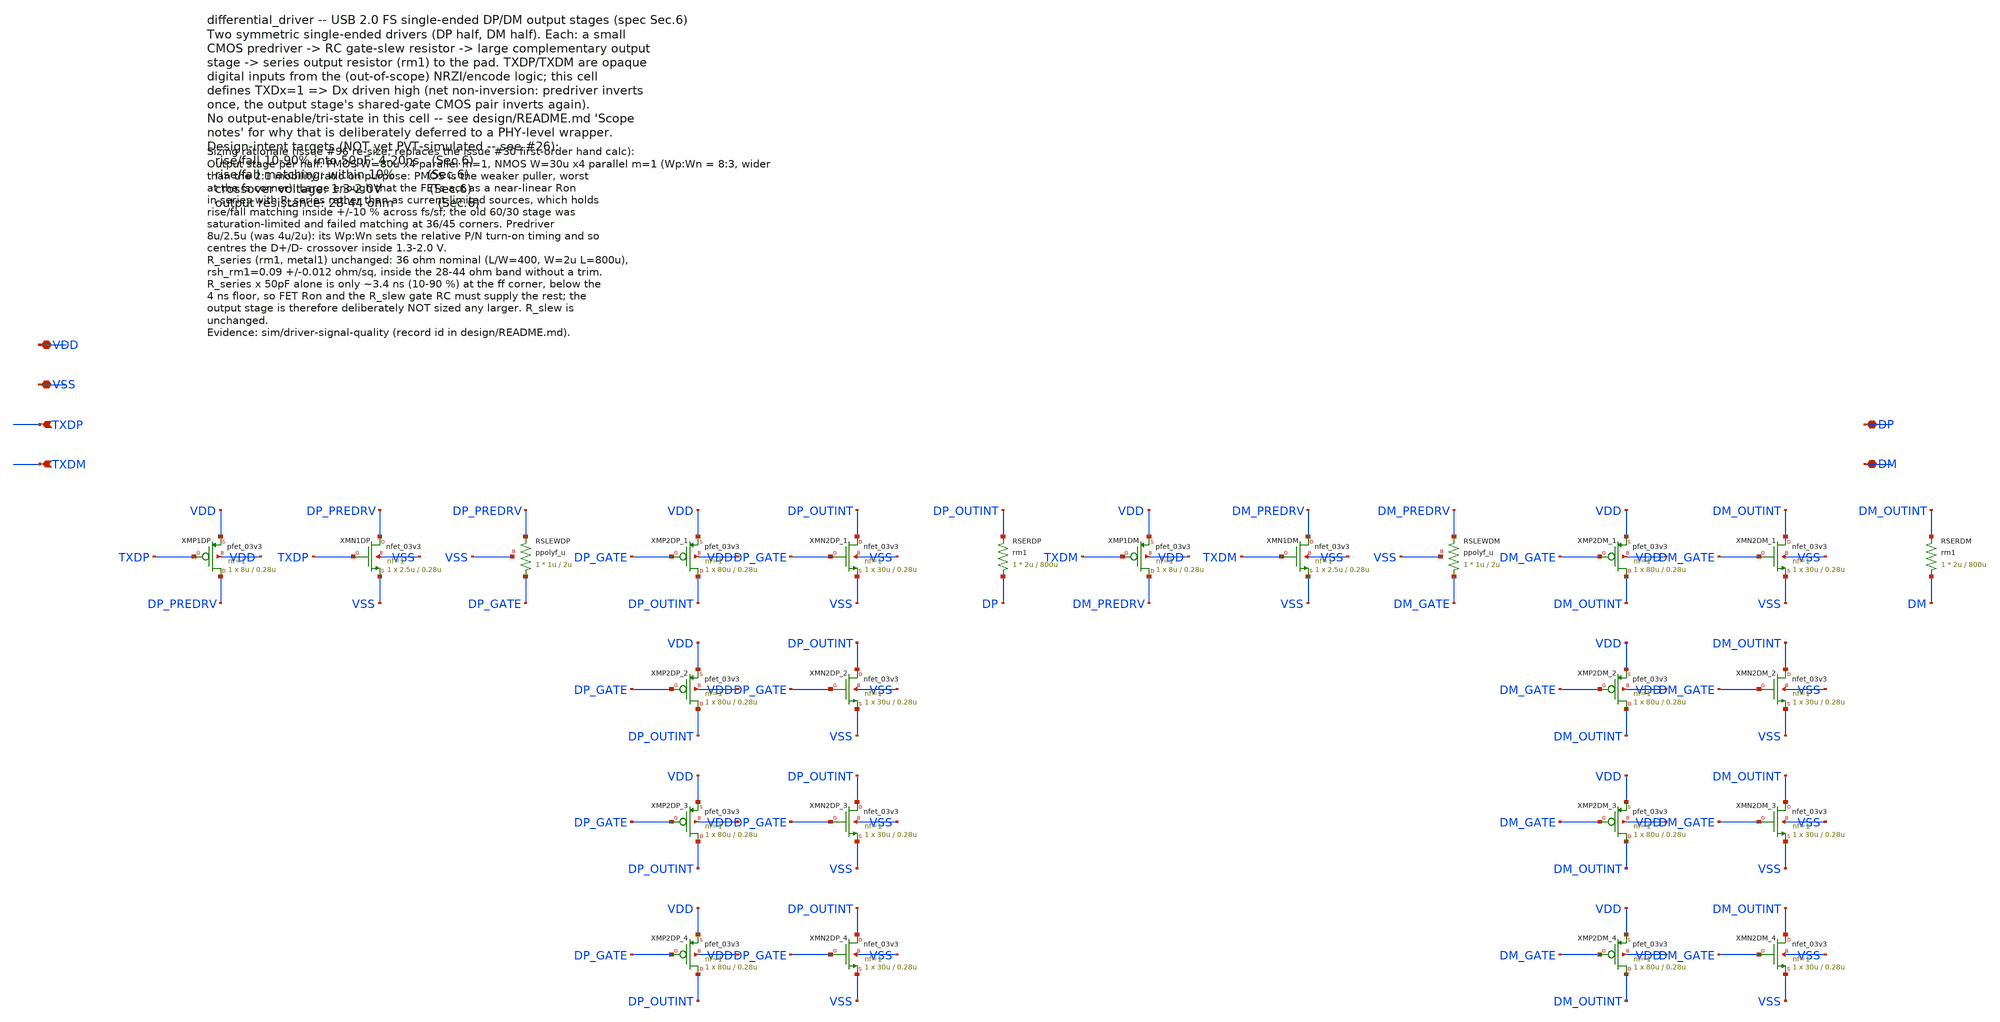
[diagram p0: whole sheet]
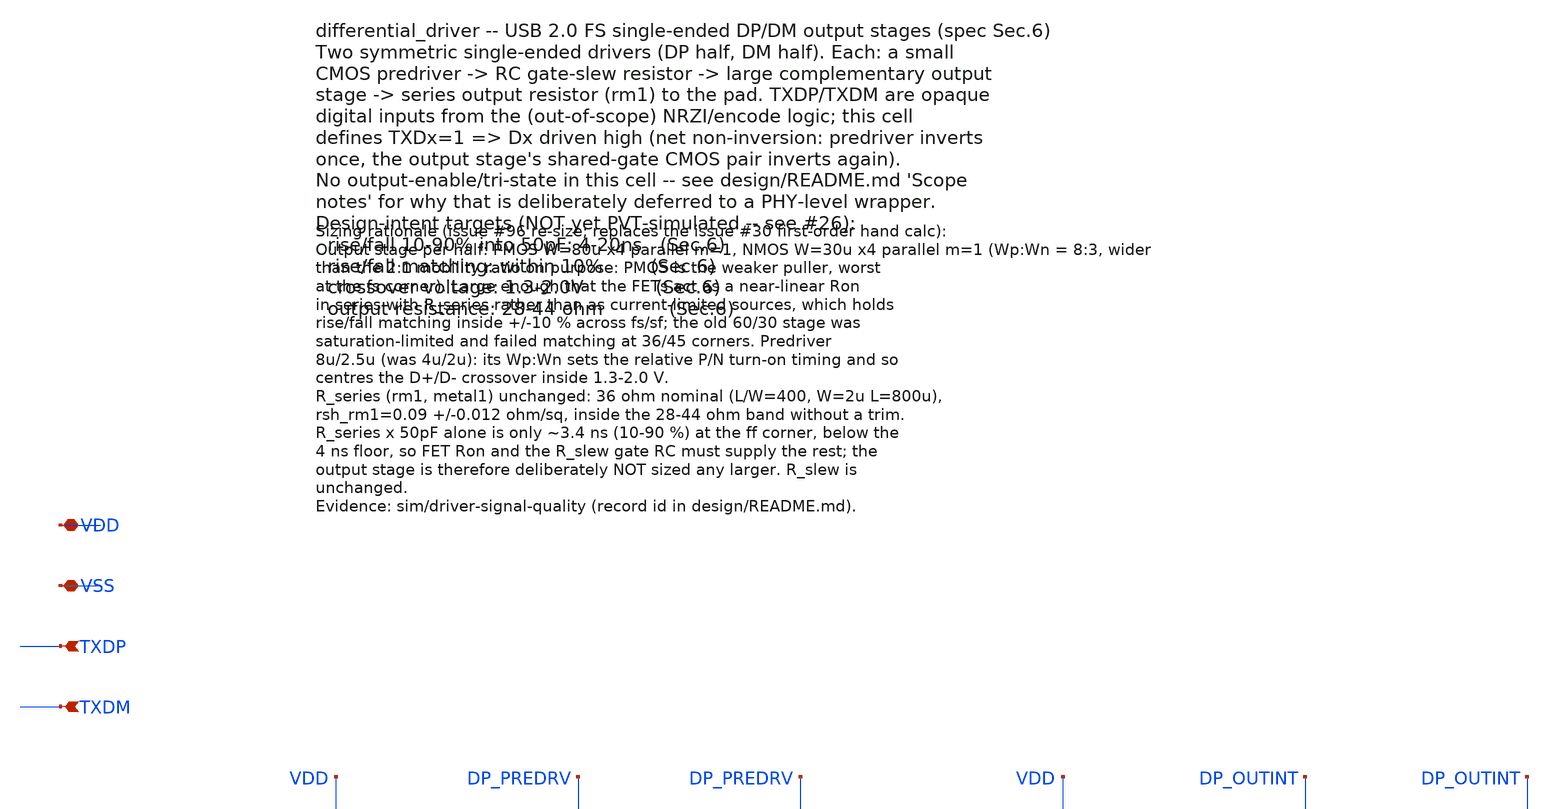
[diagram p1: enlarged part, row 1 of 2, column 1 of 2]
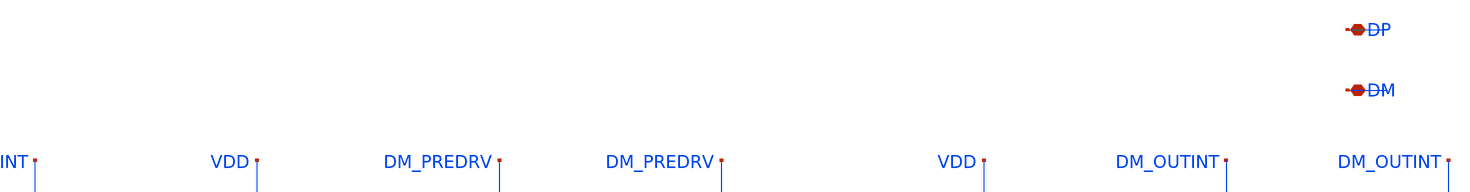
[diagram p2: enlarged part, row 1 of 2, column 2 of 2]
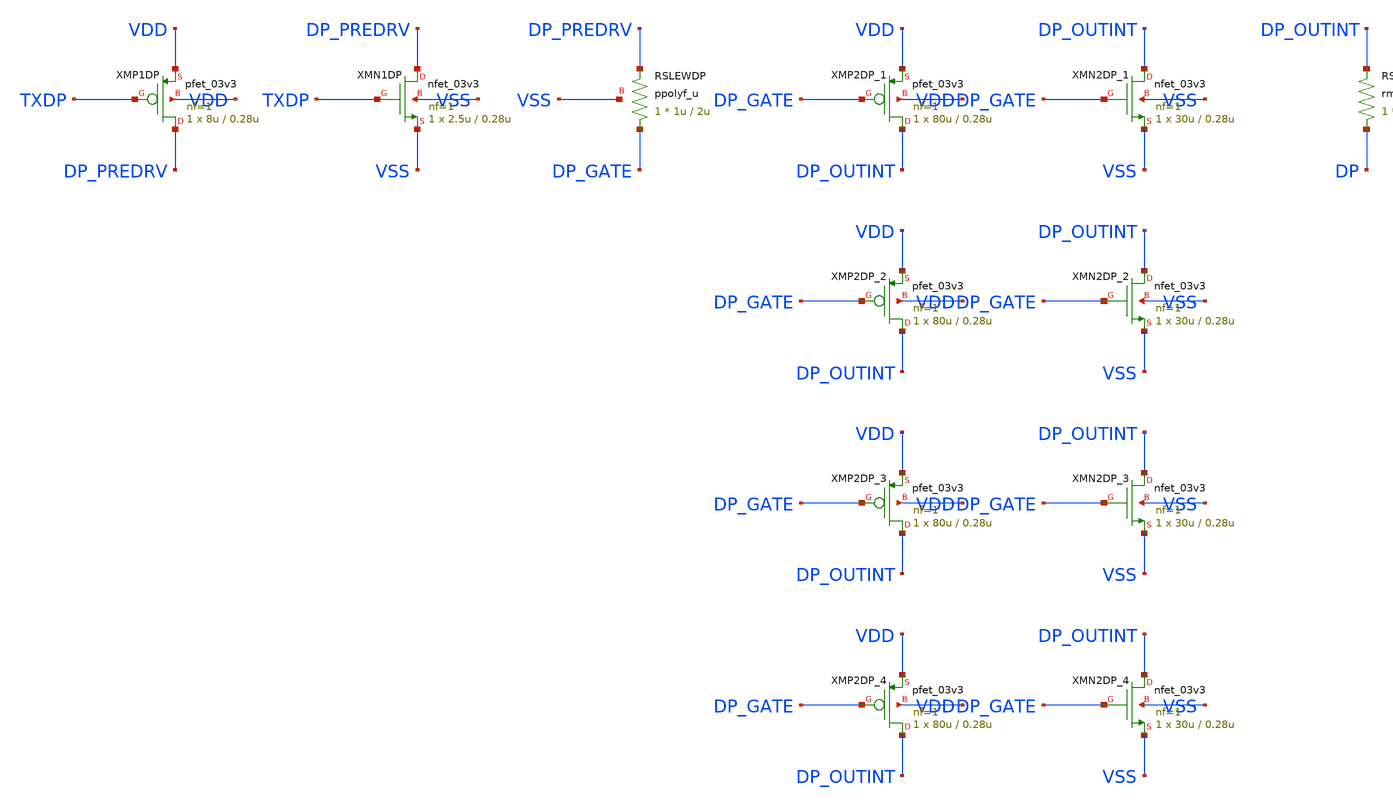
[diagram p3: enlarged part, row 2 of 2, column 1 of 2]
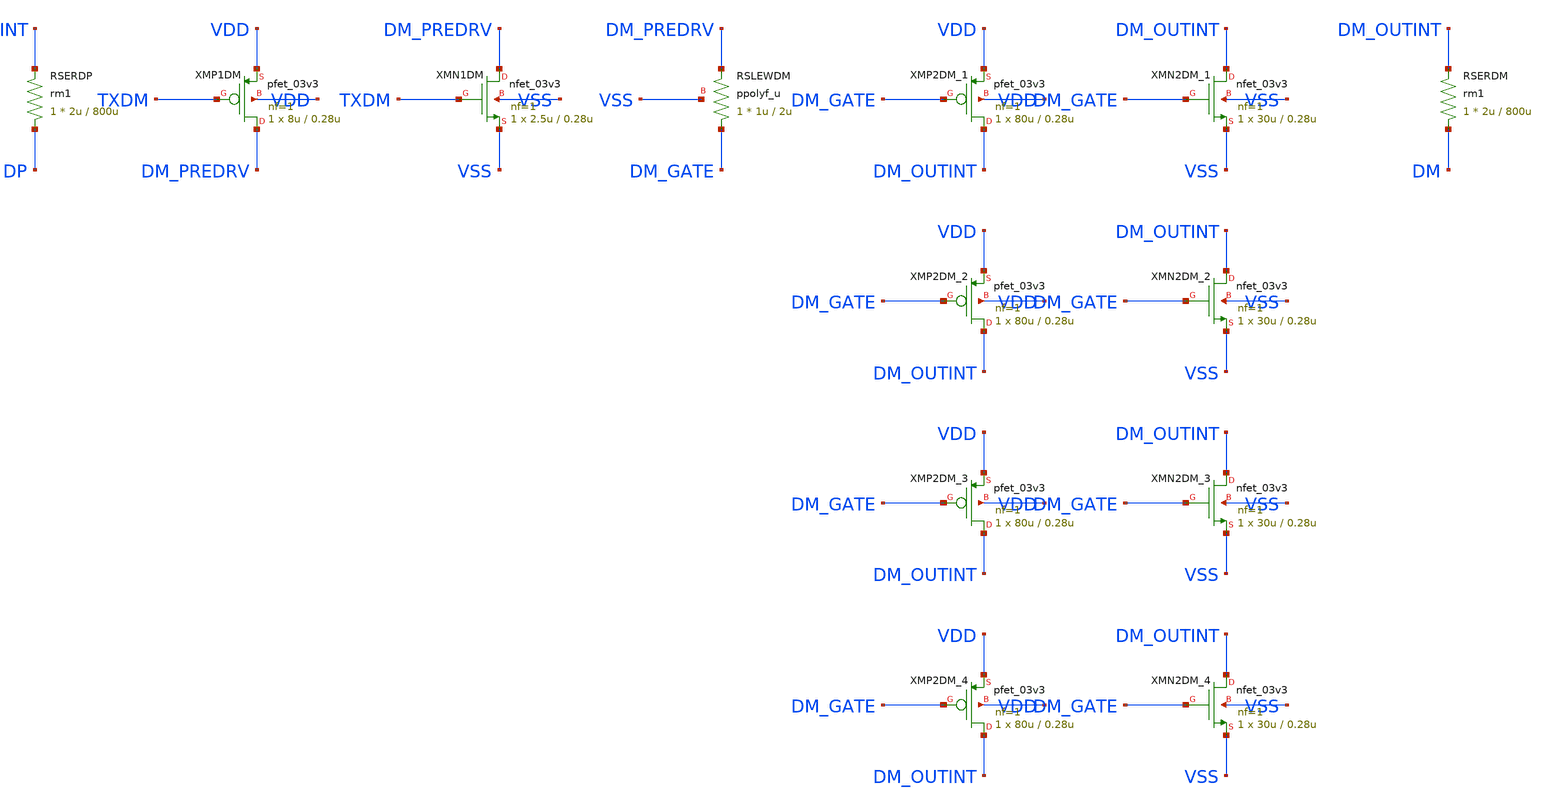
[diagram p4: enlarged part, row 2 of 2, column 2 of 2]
** sch_path: design/differential_driver.sch
**.subckt differential_driver VDD VSS TXDP TXDM DP DM
*.iopin VDD
*.iopin VSS
*.ipin TXDP
*.ipin TXDM
*.iopin DP
*.iopin DM
XMP1DP DP_PREDRV TXDP VDD VDD pfet_03v3 L=0.28u W=8u nf=1 ad='int((nf+1)/2) * W/nf * 0.18u' as='int((nf+2)/2) * W/nf * 0.18u'
+ pd='2*int((nf+1)/2) * (W/nf + 0.18u)' ps='2*int((nf+2)/2) * (W/nf + 0.18u)' nrd='0.18u / W' nrs='0.18u / W'
+ sa=0 sb=0 sd=0 m=1
XMN1DP DP_PREDRV TXDP VSS VSS nfet_03v3 L=0.28u W=2.5u nf=1 ad='int((nf+1)/2) * W/nf * 0.18u' as='int((nf+2)/2) * W/nf * 0.18u'
+ pd='2*int((nf+1)/2) * (W/nf + 0.18u)' ps='2*int((nf+2)/2) * (W/nf + 0.18u)' nrd='0.18u / W' nrs='0.18u / W'
+ sa=0 sb=0 sd=0 m=1
XRSLEWDP DP_GATE DP_PREDRV VSS ppolyf_u r_width=1u r_length=2u m=1
XMP2DP_1 DP_OUTINT DP_GATE VDD VDD pfet_03v3 L=0.28u W=80u nf=1 ad='int((nf+1)/2) * W/nf * 0.18u' as='int((nf+2)/2) * W/nf * 0.18u'
+ pd='2*int((nf+1)/2) * (W/nf + 0.18u)' ps='2*int((nf+2)/2) * (W/nf + 0.18u)' nrd='0.18u / W' nrs='0.18u / W'
+ sa=0 sb=0 sd=0 m=1
XMP2DP_2 DP_OUTINT DP_GATE VDD VDD pfet_03v3 L=0.28u W=80u nf=1 ad='int((nf+1)/2) * W/nf * 0.18u' as='int((nf+2)/2) * W/nf * 0.18u'
+ pd='2*int((nf+1)/2) * (W/nf + 0.18u)' ps='2*int((nf+2)/2) * (W/nf + 0.18u)' nrd='0.18u / W' nrs='0.18u / W'
+ sa=0 sb=0 sd=0 m=1
XMP2DP_3 DP_OUTINT DP_GATE VDD VDD pfet_03v3 L=0.28u W=80u nf=1 ad='int((nf+1)/2) * W/nf * 0.18u' as='int((nf+2)/2) * W/nf * 0.18u'
+ pd='2*int((nf+1)/2) * (W/nf + 0.18u)' ps='2*int((nf+2)/2) * (W/nf + 0.18u)' nrd='0.18u / W' nrs='0.18u / W'
+ sa=0 sb=0 sd=0 m=1
XMP2DP_4 DP_OUTINT DP_GATE VDD VDD pfet_03v3 L=0.28u W=80u nf=1 ad='int((nf+1)/2) * W/nf * 0.18u' as='int((nf+2)/2) * W/nf * 0.18u'
+ pd='2*int((nf+1)/2) * (W/nf + 0.18u)' ps='2*int((nf+2)/2) * (W/nf + 0.18u)' nrd='0.18u / W' nrs='0.18u / W'
+ sa=0 sb=0 sd=0 m=1
XMN2DP_1 DP_OUTINT DP_GATE VSS VSS nfet_03v3 L=0.28u W=30u nf=1 ad='int((nf+1)/2) * W/nf * 0.18u' as='int((nf+2)/2) * W/nf * 0.18u'
+ pd='2*int((nf+1)/2) * (W/nf + 0.18u)' ps='2*int((nf+2)/2) * (W/nf + 0.18u)' nrd='0.18u / W' nrs='0.18u / W'
+ sa=0 sb=0 sd=0 m=1
XMN2DP_2 DP_OUTINT DP_GATE VSS VSS nfet_03v3 L=0.28u W=30u nf=1 ad='int((nf+1)/2) * W/nf * 0.18u' as='int((nf+2)/2) * W/nf * 0.18u'
+ pd='2*int((nf+1)/2) * (W/nf + 0.18u)' ps='2*int((nf+2)/2) * (W/nf + 0.18u)' nrd='0.18u / W' nrs='0.18u / W'
+ sa=0 sb=0 sd=0 m=1
XMN2DP_3 DP_OUTINT DP_GATE VSS VSS nfet_03v3 L=0.28u W=30u nf=1 ad='int((nf+1)/2) * W/nf * 0.18u' as='int((nf+2)/2) * W/nf * 0.18u'
+ pd='2*int((nf+1)/2) * (W/nf + 0.18u)' ps='2*int((nf+2)/2) * (W/nf + 0.18u)' nrd='0.18u / W' nrs='0.18u / W'
+ sa=0 sb=0 sd=0 m=1
XMN2DP_4 DP_OUTINT DP_GATE VSS VSS nfet_03v3 L=0.28u W=30u nf=1 ad='int((nf+1)/2) * W/nf * 0.18u' as='int((nf+2)/2) * W/nf * 0.18u'
+ pd='2*int((nf+1)/2) * (W/nf + 0.18u)' ps='2*int((nf+2)/2) * (W/nf + 0.18u)' nrd='0.18u / W' nrs='0.18u / W'
+ sa=0 sb=0 sd=0 m=1
XRSERDP DP DP_OUTINT rm1 r_width=2u r_length=800u m=1
XMP1DM DM_PREDRV TXDM VDD VDD pfet_03v3 L=0.28u W=8u nf=1 ad='int((nf+1)/2) * W/nf * 0.18u' as='int((nf+2)/2) * W/nf * 0.18u'
+ pd='2*int((nf+1)/2) * (W/nf + 0.18u)' ps='2*int((nf+2)/2) * (W/nf + 0.18u)' nrd='0.18u / W' nrs='0.18u / W'
+ sa=0 sb=0 sd=0 m=1
XMN1DM DM_PREDRV TXDM VSS VSS nfet_03v3 L=0.28u W=2.5u nf=1 ad='int((nf+1)/2) * W/nf * 0.18u' as='int((nf+2)/2) * W/nf * 0.18u'
+ pd='2*int((nf+1)/2) * (W/nf + 0.18u)' ps='2*int((nf+2)/2) * (W/nf + 0.18u)' nrd='0.18u / W' nrs='0.18u / W'
+ sa=0 sb=0 sd=0 m=1
XRSLEWDM DM_GATE DM_PREDRV VSS ppolyf_u r_width=1u r_length=2u m=1
XMP2DM_1 DM_OUTINT DM_GATE VDD VDD pfet_03v3 L=0.28u W=80u nf=1 ad='int((nf+1)/2) * W/nf * 0.18u' as='int((nf+2)/2) * W/nf * 0.18u'
+ pd='2*int((nf+1)/2) * (W/nf + 0.18u)' ps='2*int((nf+2)/2) * (W/nf + 0.18u)' nrd='0.18u / W' nrs='0.18u / W'
+ sa=0 sb=0 sd=0 m=1
XMP2DM_2 DM_OUTINT DM_GATE VDD VDD pfet_03v3 L=0.28u W=80u nf=1 ad='int((nf+1)/2) * W/nf * 0.18u' as='int((nf+2)/2) * W/nf * 0.18u'
+ pd='2*int((nf+1)/2) * (W/nf + 0.18u)' ps='2*int((nf+2)/2) * (W/nf + 0.18u)' nrd='0.18u / W' nrs='0.18u / W'
+ sa=0 sb=0 sd=0 m=1
XMP2DM_3 DM_OUTINT DM_GATE VDD VDD pfet_03v3 L=0.28u W=80u nf=1 ad='int((nf+1)/2) * W/nf * 0.18u' as='int((nf+2)/2) * W/nf * 0.18u'
+ pd='2*int((nf+1)/2) * (W/nf + 0.18u)' ps='2*int((nf+2)/2) * (W/nf + 0.18u)' nrd='0.18u / W' nrs='0.18u / W'
+ sa=0 sb=0 sd=0 m=1
XMP2DM_4 DM_OUTINT DM_GATE VDD VDD pfet_03v3 L=0.28u W=80u nf=1 ad='int((nf+1)/2) * W/nf * 0.18u' as='int((nf+2)/2) * W/nf * 0.18u'
+ pd='2*int((nf+1)/2) * (W/nf + 0.18u)' ps='2*int((nf+2)/2) * (W/nf + 0.18u)' nrd='0.18u / W' nrs='0.18u / W'
+ sa=0 sb=0 sd=0 m=1
XMN2DM_1 DM_OUTINT DM_GATE VSS VSS nfet_03v3 L=0.28u W=30u nf=1 ad='int((nf+1)/2) * W/nf * 0.18u' as='int((nf+2)/2) * W/nf * 0.18u'
+ pd='2*int((nf+1)/2) * (W/nf + 0.18u)' ps='2*int((nf+2)/2) * (W/nf + 0.18u)' nrd='0.18u / W' nrs='0.18u / W'
+ sa=0 sb=0 sd=0 m=1
XMN2DM_2 DM_OUTINT DM_GATE VSS VSS nfet_03v3 L=0.28u W=30u nf=1 ad='int((nf+1)/2) * W/nf * 0.18u' as='int((nf+2)/2) * W/nf * 0.18u'
+ pd='2*int((nf+1)/2) * (W/nf + 0.18u)' ps='2*int((nf+2)/2) * (W/nf + 0.18u)' nrd='0.18u / W' nrs='0.18u / W'
+ sa=0 sb=0 sd=0 m=1
XMN2DM_3 DM_OUTINT DM_GATE VSS VSS nfet_03v3 L=0.28u W=30u nf=1 ad='int((nf+1)/2) * W/nf * 0.18u' as='int((nf+2)/2) * W/nf * 0.18u'
+ pd='2*int((nf+1)/2) * (W/nf + 0.18u)' ps='2*int((nf+2)/2) * (W/nf + 0.18u)' nrd='0.18u / W' nrs='0.18u / W'
+ sa=0 sb=0 sd=0 m=1
XMN2DM_4 DM_OUTINT DM_GATE VSS VSS nfet_03v3 L=0.28u W=30u nf=1 ad='int((nf+1)/2) * W/nf * 0.18u' as='int((nf+2)/2) * W/nf * 0.18u'
+ pd='2*int((nf+1)/2) * (W/nf + 0.18u)' ps='2*int((nf+2)/2) * (W/nf + 0.18u)' nrd='0.18u / W' nrs='0.18u / W'
+ sa=0 sb=0 sd=0 m=1
XRSERDM DM DM_OUTINT rm1 r_width=2u r_length=800u m=1
**.ends
.end
